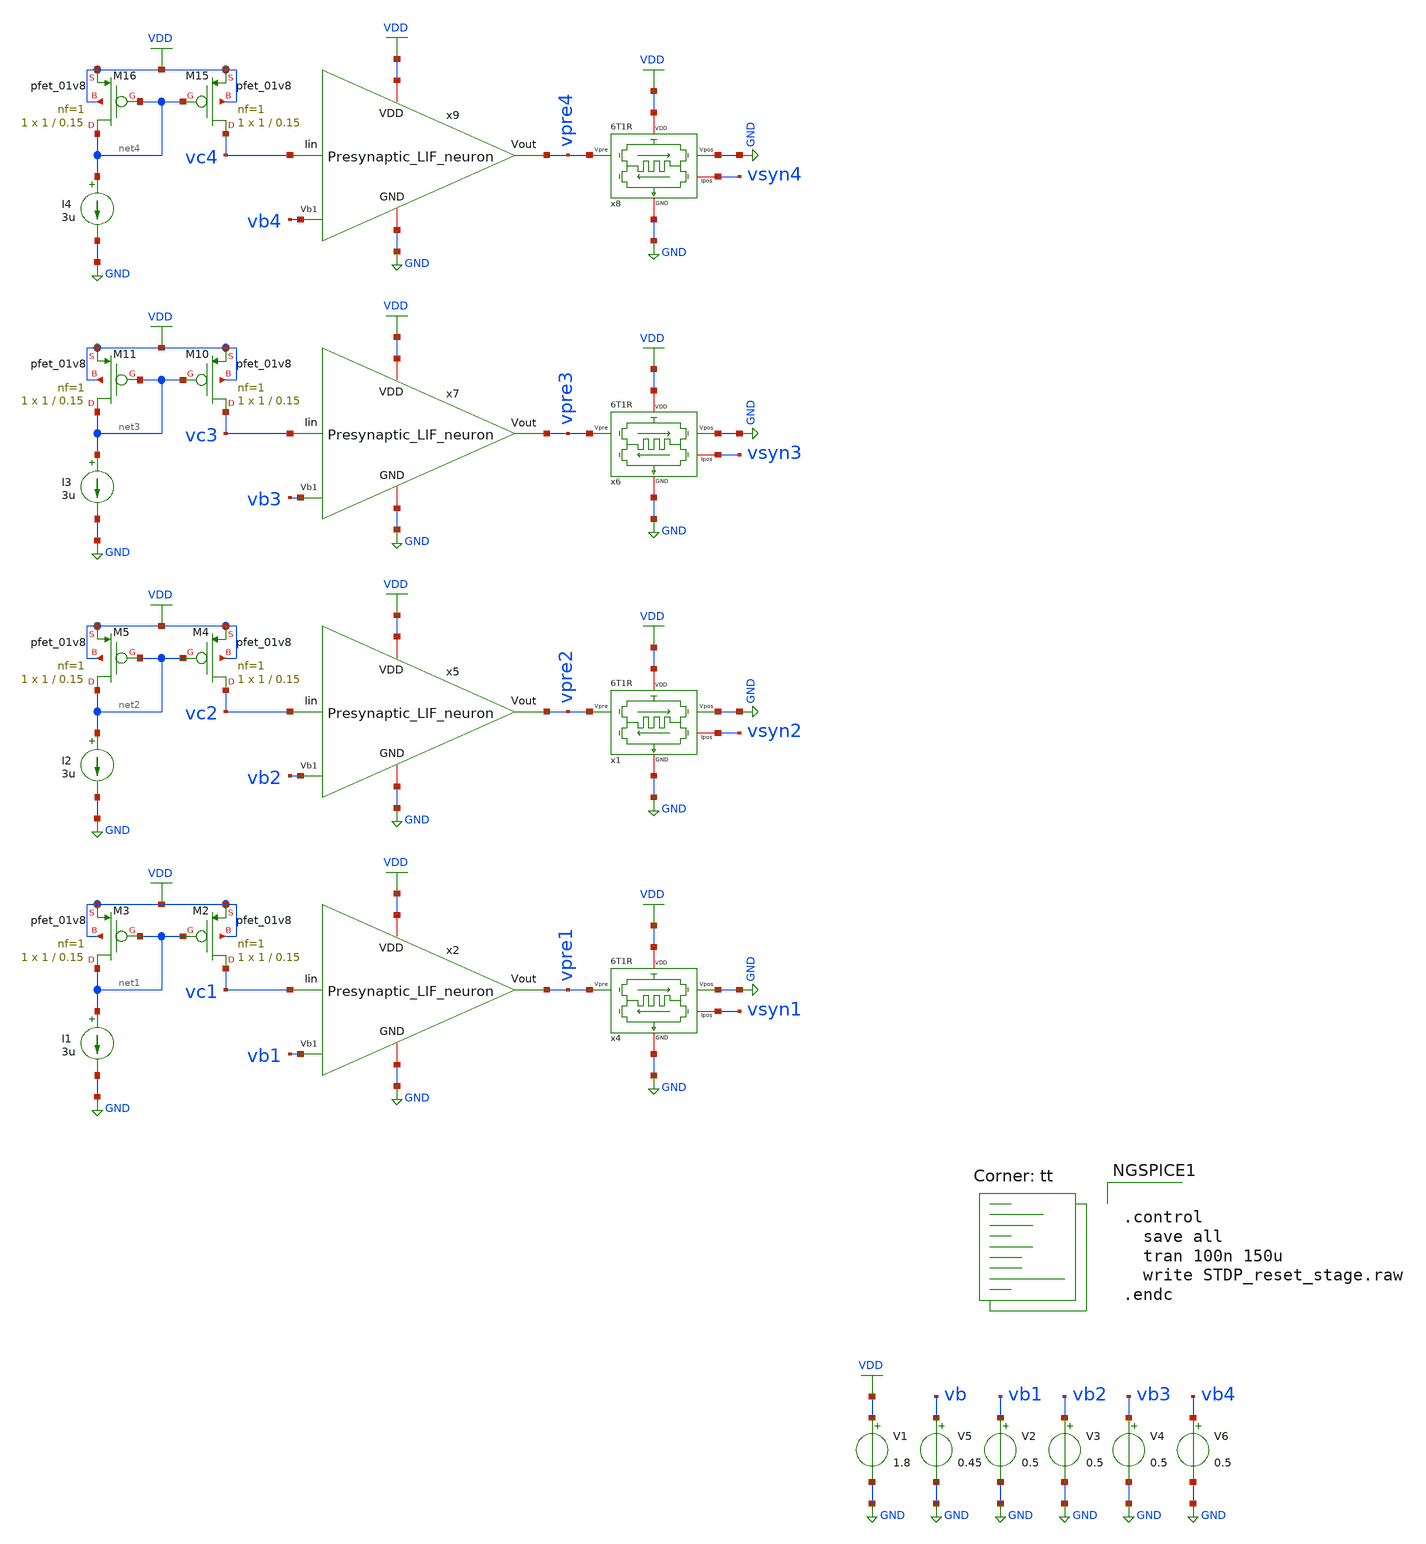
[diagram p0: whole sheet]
** sch_path: STDP/STDP_reset_stage.sch
**.subckt STDP_reset_stage
V1 VDD GND 1.8
V2 vb1 GND 0.5
x4 VDD vsyn1 vpre1 GND GND 6T1R
I1 net1 GND 3u
XM2 vc1 net1 VDD VDD sky130_fd_pr__pfet_01v8 L=0.15 W=1 nf=1 ad='int((nf+1)/2) * W/nf * 0.29' as='int((nf+2)/2) * W/nf * 0.29'
+ pd='2*int((nf+1)/2) * (W/nf + 0.29)' ps='2*int((nf+2)/2) * (W/nf + 0.29)' nrd='0.29 / W' nrs='0.29 / W'
+ sa=0 sb=0 sd=0 mult=1 m=1
XM3 net1 net1 VDD VDD sky130_fd_pr__pfet_01v8 L=0.15 W=1 nf=1 ad='int((nf+1)/2) * W/nf * 0.29' as='int((nf+2)/2) * W/nf * 0.29'
+ pd='2*int((nf+1)/2) * (W/nf + 0.29)' ps='2*int((nf+2)/2) * (W/nf + 0.29)' nrd='0.29 / W' nrs='0.29 / W'
+ sa=0 sb=0 sd=0 mult=1 m=1
V3 vb2 GND 0.5
V4 vb3 GND 0.5
x2 VDD vpre1 vb1 GND vc1 Presynaptic_LIF_neuron
V5 vb GND 0.45
x1 VDD vsyn2 vpre2 GND GND 6T1R
x5 VDD vpre2 vb2 GND vc2 Presynaptic_LIF_neuron
I2 net2 GND 3u
XM4 vc2 net2 VDD VDD sky130_fd_pr__pfet_01v8 L=0.15 W=1 nf=1 ad='int((nf+1)/2) * W/nf * 0.29' as='int((nf+2)/2) * W/nf * 0.29'
+ pd='2*int((nf+1)/2) * (W/nf + 0.29)' ps='2*int((nf+2)/2) * (W/nf + 0.29)' nrd='0.29 / W' nrs='0.29 / W'
+ sa=0 sb=0 sd=0 mult=1 m=1
XM5 net2 net2 VDD VDD sky130_fd_pr__pfet_01v8 L=0.15 W=1 nf=1 ad='int((nf+1)/2) * W/nf * 0.29' as='int((nf+2)/2) * W/nf * 0.29'
+ pd='2*int((nf+1)/2) * (W/nf + 0.29)' ps='2*int((nf+2)/2) * (W/nf + 0.29)' nrd='0.29 / W' nrs='0.29 / W'
+ sa=0 sb=0 sd=0 mult=1 m=1
x6 VDD vsyn3 vpre3 GND GND 6T1R
x7 VDD vpre3 vb3 GND vc3 Presynaptic_LIF_neuron
I3 net3 GND 3u
XM10 vc3 net3 VDD VDD sky130_fd_pr__pfet_01v8 L=0.15 W=1 nf=1 ad='int((nf+1)/2) * W/nf * 0.29' as='int((nf+2)/2) * W/nf * 0.29'
+ pd='2*int((nf+1)/2) * (W/nf + 0.29)' ps='2*int((nf+2)/2) * (W/nf + 0.29)' nrd='0.29 / W' nrs='0.29 / W'
+ sa=0 sb=0 sd=0 mult=1 m=1
XM11 net3 net3 VDD VDD sky130_fd_pr__pfet_01v8 L=0.15 W=1 nf=1 ad='int((nf+1)/2) * W/nf * 0.29' as='int((nf+2)/2) * W/nf * 0.29'
+ pd='2*int((nf+1)/2) * (W/nf + 0.29)' ps='2*int((nf+2)/2) * (W/nf + 0.29)' nrd='0.29 / W' nrs='0.29 / W'
+ sa=0 sb=0 sd=0 mult=1 m=1
x8 VDD vsyn4 vpre4 GND GND 6T1R
x9 VDD vpre4 vb4 GND vc4 Presynaptic_LIF_neuron
I4 net4 GND 3u
XM15 vc4 net4 VDD VDD sky130_fd_pr__pfet_01v8 L=0.15 W=1 nf=1 ad='int((nf+1)/2) * W/nf * 0.29' as='int((nf+2)/2) * W/nf * 0.29'
+ pd='2*int((nf+1)/2) * (W/nf + 0.29)' ps='2*int((nf+2)/2) * (W/nf + 0.29)' nrd='0.29 / W' nrs='0.29 / W'
+ sa=0 sb=0 sd=0 mult=1 m=1
XM16 net4 net4 VDD VDD sky130_fd_pr__pfet_01v8 L=0.15 W=1 nf=1 ad='int((nf+1)/2) * W/nf * 0.29' as='int((nf+2)/2) * W/nf * 0.29'
+ pd='2*int((nf+1)/2) * (W/nf + 0.29)' ps='2*int((nf+2)/2) * (W/nf + 0.29)' nrd='0.29 / W' nrs='0.29 / W'
+ sa=0 sb=0 sd=0 mult=1 m=1
V6 vb4 GND 0.5
**** begin user architecture code
.lib $::SKYWATER_MODELS/sky130.lib.spice tt

** opencircuitdesign pdks install
.inc $::SKYWATER_MODELS/rram_v0.spice



.control
  save all
  tran 100n 150u
  write STDP_reset_stage.raw
.endc


**** end user architecture code
**.ends

* expanding   symbol:  /home/ricardo/RATT_repos/Proyectos_xschem/synapse/6T1R.sym # of pins=5
** sym_path: synapse/6T1R.sym
** sch_path: synapse/6T1R.sch
.subckt 6T1R VDD Ipos Vpre Vpos GND
*.ipin Vpre
*.ipin Vpos
*.iopin GND
*.iopin Ipos
*.iopin VDD
XM1 vipre Vpre net1 GND sky130_fd_pr__nfet_01v8 L=0.15 W=10 nf=1 ad='int((nf+1)/2) * W/nf * 0.29' as='int((nf+2)/2) * W/nf * 0.29'
+ pd='2*int((nf+1)/2) * (W/nf + 0.29)' ps='2*int((nf+2)/2) * (W/nf + 0.29)' nrd='0.29 / W' nrs='0.29 / W'
+ sa=0 sb=0 sd=0 mult=1 m=1
XR1 net2 net1 rram_v0
XM3 vipre Vpos net2 GND sky130_fd_pr__nfet_01v8 L=0.15 W=1 nf=1 ad='int((nf+1)/2) * W/nf * 0.29' as='int((nf+2)/2) * W/nf * 0.29'
+ pd='2*int((nf+1)/2) * (W/nf + 0.29)' ps='2*int((nf+2)/2) * (W/nf + 0.29)' nrd='0.29 / W' nrs='0.29 / W'
+ sa=0 sb=0 sd=0 mult=1 m=1
XM6 Ipos vipre VDD VDD sky130_fd_pr__pfet_01v8 L=0.15 W=1 nf=1 ad='int((nf+1)/2) * W/nf * 0.29' as='int((nf+2)/2) * W/nf * 0.29'
+ pd='2*int((nf+1)/2) * (W/nf + 0.29)' ps='2*int((nf+2)/2) * (W/nf + 0.29)' nrd='0.29 / W' nrs='0.29 / W'
+ sa=0 sb=0 sd=0 mult=1 m=1
XM5 vipre vipre VDD VDD sky130_fd_pr__pfet_01v8 L=0.15 W=20 nf=1 ad='int((nf+1)/2) * W/nf * 0.29' as='int((nf+2)/2) * W/nf * 0.29'
+ pd='2*int((nf+1)/2) * (W/nf + 0.29)' ps='2*int((nf+2)/2) * (W/nf + 0.29)' nrd='0.29 / W' nrs='0.29 / W'
+ sa=0 sb=0 sd=0 mult=1 m=1
XM2 net1 Vpos GND GND sky130_fd_pr__nfet_01v8 L=0.15 W=1 nf=1 ad='int((nf+1)/2) * W/nf * 0.29' as='int((nf+2)/2) * W/nf * 0.29'
+ pd='2*int((nf+1)/2) * (W/nf + 0.29)' ps='2*int((nf+2)/2) * (W/nf + 0.29)' nrd='0.29 / W' nrs='0.29 / W'
+ sa=0 sb=0 sd=0 mult=1 m=1
XM4 net2 Vpre GND GND sky130_fd_pr__nfet_01v8 L=0.15 W=10 nf=1 ad='int((nf+1)/2) * W/nf * 0.29' as='int((nf+2)/2) * W/nf * 0.29'
+ pd='2*int((nf+1)/2) * (W/nf + 0.29)' ps='2*int((nf+2)/2) * (W/nf + 0.29)' nrd='0.29 / W' nrs='0.29 / W'
+ sa=0 sb=0 sd=0 mult=1 m=1
.ends


* expanding   symbol:
*+  /home/ricardo/RATT_repos/Proyectos_xschem/LIF_neuron/Presynaptic_LIF_neuron.sym # of pins=5
** sym_path: LIF_neuron/Presynaptic_LIF_neuron.sym
** sch_path: LIF_neuron/Presynaptic_LIF_neuron.sch
.subckt Presynaptic_LIF_neuron VDD Vout Vb1 GND Iin
*.iopin GND
*.ipin Vb1
*.iopin VDD
*.opin Vout
*.ipin Iin
XM13 net2 Vb1 GND GND sky130_fd_pr__nfet_01v8 L=0.5 W=5 nf=1 ad='int((nf+1)/2) * W/nf * 0.29' as='int((nf+2)/2) * W/nf * 0.29'
+ pd='2*int((nf+1)/2) * (W/nf + 0.29)' ps='2*int((nf+2)/2) * (W/nf + 0.29)' nrd='0.29 / W' nrs='0.29 / W'
+ sa=0 sb=0 sd=0 mult=1 m=1
XM12 Crefr net1 net2 GND sky130_fd_pr__nfet_01v8 L=1 W=1 nf=1 ad='int((nf+1)/2) * W/nf * 0.29' as='int((nf+2)/2) * W/nf * 0.29'
+ pd='2*int((nf+1)/2) * (W/nf + 0.29)' ps='2*int((nf+2)/2) * (W/nf + 0.29)' nrd='0.29 / W' nrs='0.29 / W'
+ sa=0 sb=0 sd=0 mult=1 m=1
XM11 Crefr net1 VDD VDD sky130_fd_pr__pfet_01v8 L=1 W=1 nf=1 ad='int((nf+1)/2) * W/nf * 0.29' as='int((nf+2)/2) * W/nf * 0.29'
+ pd='2*int((nf+1)/2) * (W/nf + 0.29)' ps='2*int((nf+2)/2) * (W/nf + 0.29)' nrd='0.29 / W' nrs='0.29 / W'
+ sa=0 sb=0 sd=0 mult=1 m=1
XCrefr Crefr GND sky130_fd_pr__cap_mim_m3_1 W=10 L=1 MF=1 m=1
XM14 Iin Crefr GND GND sky130_fd_pr__nfet_01v8 L=7 W=0.45 nf=1 ad='int((nf+1)/2) * W/nf * 0.29' as='int((nf+2)/2) * W/nf * 0.29'
+ pd='2*int((nf+1)/2) * (W/nf + 0.29)' ps='2*int((nf+2)/2) * (W/nf + 0.29)' nrd='0.29 / W' nrs='0.29 / W'
+ sa=0 sb=0 sd=0 mult=1 m=1
XCm Iin GND sky130_fd_pr__cap_mim_m3_1 W=10 L=1 MF=10 m=10
XM6 net3 Vout GND GND sky130_fd_pr__nfet_01v8 L=0.5 W=1 nf=1 ad='int((nf+1)/2) * W/nf * 0.29' as='int((nf+2)/2) * W/nf * 0.29'
+ pd='2*int((nf+1)/2) * (W/nf + 0.29)' ps='2*int((nf+2)/2) * (W/nf + 0.29)' nrd='0.29 / W' nrs='0.29 / W'
+ sa=0 sb=0 sd=0 mult=1 m=1
XM7 net1 Iin net3 GND sky130_fd_pr__nfet_01v8 L=1 W=1 nf=1 ad='int((nf+1)/2) * W/nf * 0.29' as='int((nf+2)/2) * W/nf * 0.29'
+ pd='2*int((nf+1)/2) * (W/nf + 0.29)' ps='2*int((nf+2)/2) * (W/nf + 0.29)' nrd='0.29 / W' nrs='0.29 / W'
+ sa=0 sb=0 sd=0 mult=1 m=1
XM8 net1 Iin VDD VDD sky130_fd_pr__pfet_01v8 L=1 W=1 nf=1 ad='int((nf+1)/2) * W/nf * 0.29' as='int((nf+2)/2) * W/nf * 0.29'
+ pd='2*int((nf+1)/2) * (W/nf + 0.29)' ps='2*int((nf+2)/2) * (W/nf + 0.29)' nrd='0.29 / W' nrs='0.29 / W'
+ sa=0 sb=0 sd=0 mult=1 m=1
XM9 Vout net1 net3 GND sky130_fd_pr__nfet_01v8 L=1 W=1 nf=1 ad='int((nf+1)/2) * W/nf * 0.29' as='int((nf+2)/2) * W/nf * 0.29'
+ pd='2*int((nf+1)/2) * (W/nf + 0.29)' ps='2*int((nf+2)/2) * (W/nf + 0.29)' nrd='0.29 / W' nrs='0.29 / W'
+ sa=0 sb=0 sd=0 mult=1 m=1
XM10 Vout net1 VDD VDD sky130_fd_pr__pfet_01v8 L=1 W=5 nf=1 ad='int((nf+1)/2) * W/nf * 0.29' as='int((nf+2)/2) * W/nf * 0.29'
+ pd='2*int((nf+1)/2) * (W/nf + 0.29)' ps='2*int((nf+2)/2) * (W/nf + 0.29)' nrd='0.29 / W' nrs='0.29 / W'
+ sa=0 sb=0 sd=0 mult=1 m=1
.ends

.GLOBAL GND
.GLOBAL VDD
.end
